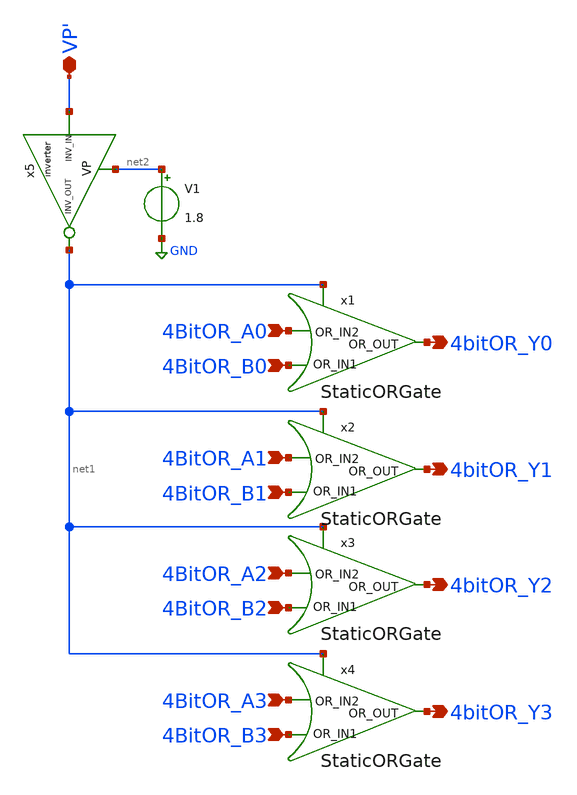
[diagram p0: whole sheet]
** sch_path: AllSymbols&Sch/4BitORNAND/4BitOR.sch
**.subckt 4BitOR 4BitOR_A0 4BitOR_B1 4BitOR_B0 4BitOR_B2 4BitOR_B3 4BitOR_A1 4BitOR_A2 4BitOR_A3 4bitOR_Y0
*+ 4bitOR_Y1 4bitOR_Y2 4bitOR_Y3 VP'
*.ipin 4BitOR_A0
*.ipin 4BitOR_B1
*.ipin 4BitOR_B0
*.ipin 4BitOR_B2
*.ipin 4BitOR_B3
*.ipin 4BitOR_A1
*.ipin 4BitOR_A2
*.ipin 4BitOR_A3
*.opin 4bitOR_Y0
*.opin 4bitOR_Y1
*.opin 4bitOR_Y2
*.opin 4bitOR_Y3
*.iopin VP'
V1 net2 GND 1.8
x1 4BitOR_A0 4BitOR_B0 4bitOR_Y0 net1 StaticORGate
x2 4BitOR_A1 4BitOR_B1 4bitOR_Y1 net1 StaticORGate
x3 4BitOR_A2 4BitOR_B2 4bitOR_Y2 net1 StaticORGate
x4 4BitOR_A3 4BitOR_B3 4bitOR_Y3 net1 StaticORGate
x5 net2 net1 VP' inverter
**.ends

* expanding   symbol:  /home/safal/projects/GitHub_CMOS_4bit_ALU/AllSymbols&Sch/Gates/StaticORGate.sym # of pins=4
** sym_path: AllSymbols&Sch/Gates/StaticORGate.sym
** sch_path: AllSymbols&Sch/Gates/StaticORGate.sch
.subckt StaticORGate OR_IN2 OR_IN1 OR_OUT VP
*.ipin OR_IN1
*.opin OR_OUT
*.ipin OR_IN2
*.iopin VP
XM1 net2 OR_IN1 net1 net1 sky130_fd_pr__pfet_01v8 L=0.15 W=8 nf=1 ad='int((1 + 1)/2) * 8 / 1 * 0.29' as='int((1
+ + 2)/2) * 8 / 1 * 0.29' pd='2*int((1 + 1)/2) * (8 / 1 + 0.29)' ps='2*int((1 + 2)/2) * (8 / 1 + 0.29)' nrd='0.29
+ / 8 ' nrs='0.29 / 8 ' sa=0 sb=0 sd=0 mult=1 m=1
XM2 net2 OR_IN1 GND GND sky130_fd_pr__nfet_01v8 L=0.15 W=1 nf=1 ad='int((1 + 1)/2) * 1 / 1 * 0.29' as='int((1
+ + 2)/2) * 1 / 1 * 0.29' pd='2*int((1 + 1)/2) * (1 / 1 + 0.29)' ps='2*int((1 + 2)/2) * (1 / 1 + 0.29)' nrd='0.29
+ / 1 ' nrs='0.29 / 1 ' sa=0 sb=0 sd=0 mult=1 m=1
XM5 net1 OR_IN2 VP VP sky130_fd_pr__pfet_01v8 L=0.15 W=8 nf=1 ad='int((1 + 1)/2) * 8 / 1 * 0.29' as='int((1
+ + 2)/2) * 8 / 1 * 0.29' pd='2*int((1 + 1)/2) * (8 / 1 + 0.29)' ps='2*int((1 + 2)/2) * (8 / 1 + 0.29)' nrd='0.29
+ / 8 ' nrs='0.29 / 8 ' sa=0 sb=0 sd=0 mult=1 m=1
XM6 net2 OR_IN2 GND GND sky130_fd_pr__nfet_01v8 L=0.15 W=1 nf=1 ad='int((1 + 1)/2) * 1 / 1 * 0.29' as='int((1
+ + 2)/2) * 1 / 1 * 0.29' pd='2*int((1 + 1)/2) * (1 / 1 + 0.29)' ps='2*int((1 + 2)/2) * (1 / 1 + 0.29)' nrd='0.29
+ / 1 ' nrs='0.29 / 1 ' sa=0 sb=0 sd=0 mult=1 m=1
x1 VP OR_OUT net2 inverter
.ends


* expanding   symbol:  /home/safal/projects/GitHub_CMOS_4bit_ALU/AllSymbols&Sch/GenericSym/inverter.sym # of pins=3
** sym_path: AllSymbols&Sch/GenericSym/inverter.sym
** sch_path: AllSymbols&Sch/GenericSym/inverter.sch
.subckt inverter VP inv_out inv_in
*.ipin inv_in
*.opin inv_out
*.iopin VP
XM1 inv_out inv_in VP VP sky130_fd_pr__pfet_01v8 L=0.15 W=2 nf=1 ad='int((1 + 1)/2) * 2 / 1 * 0.29' as='int((1
+ + 2)/2) * 2 / 1 * 0.29' pd='2*int((1 + 1)/2) * (2 / 1 + 0.29)' ps='2*int((1 + 2)/2) * (2 / 1 + 0.29)' nrd='0.29
+ / 2 ' nrs='0.29 / 2 ' sa=0 sb=0 sd=0 mult=1 m=1
XM2 inv_out inv_in GND GND sky130_fd_pr__nfet_01v8 L=0.15 W=1 nf=1 ad='int((1 + 1)/2) * 1 / 1 * 0.29' as='int((1
+ + 2)/2) * 1 / 1 * 0.29' pd='2*int((1 + 1)/2) * (1 / 1 + 0.29)' ps='2*int((1 + 2)/2) * (1 / 1 + 0.29)' nrd='0.29
+ / 1 ' nrs='0.29 / 1 ' sa=0 sb=0 sd=0 mult=1 m=1
.ends

.GLOBAL GND
.end
